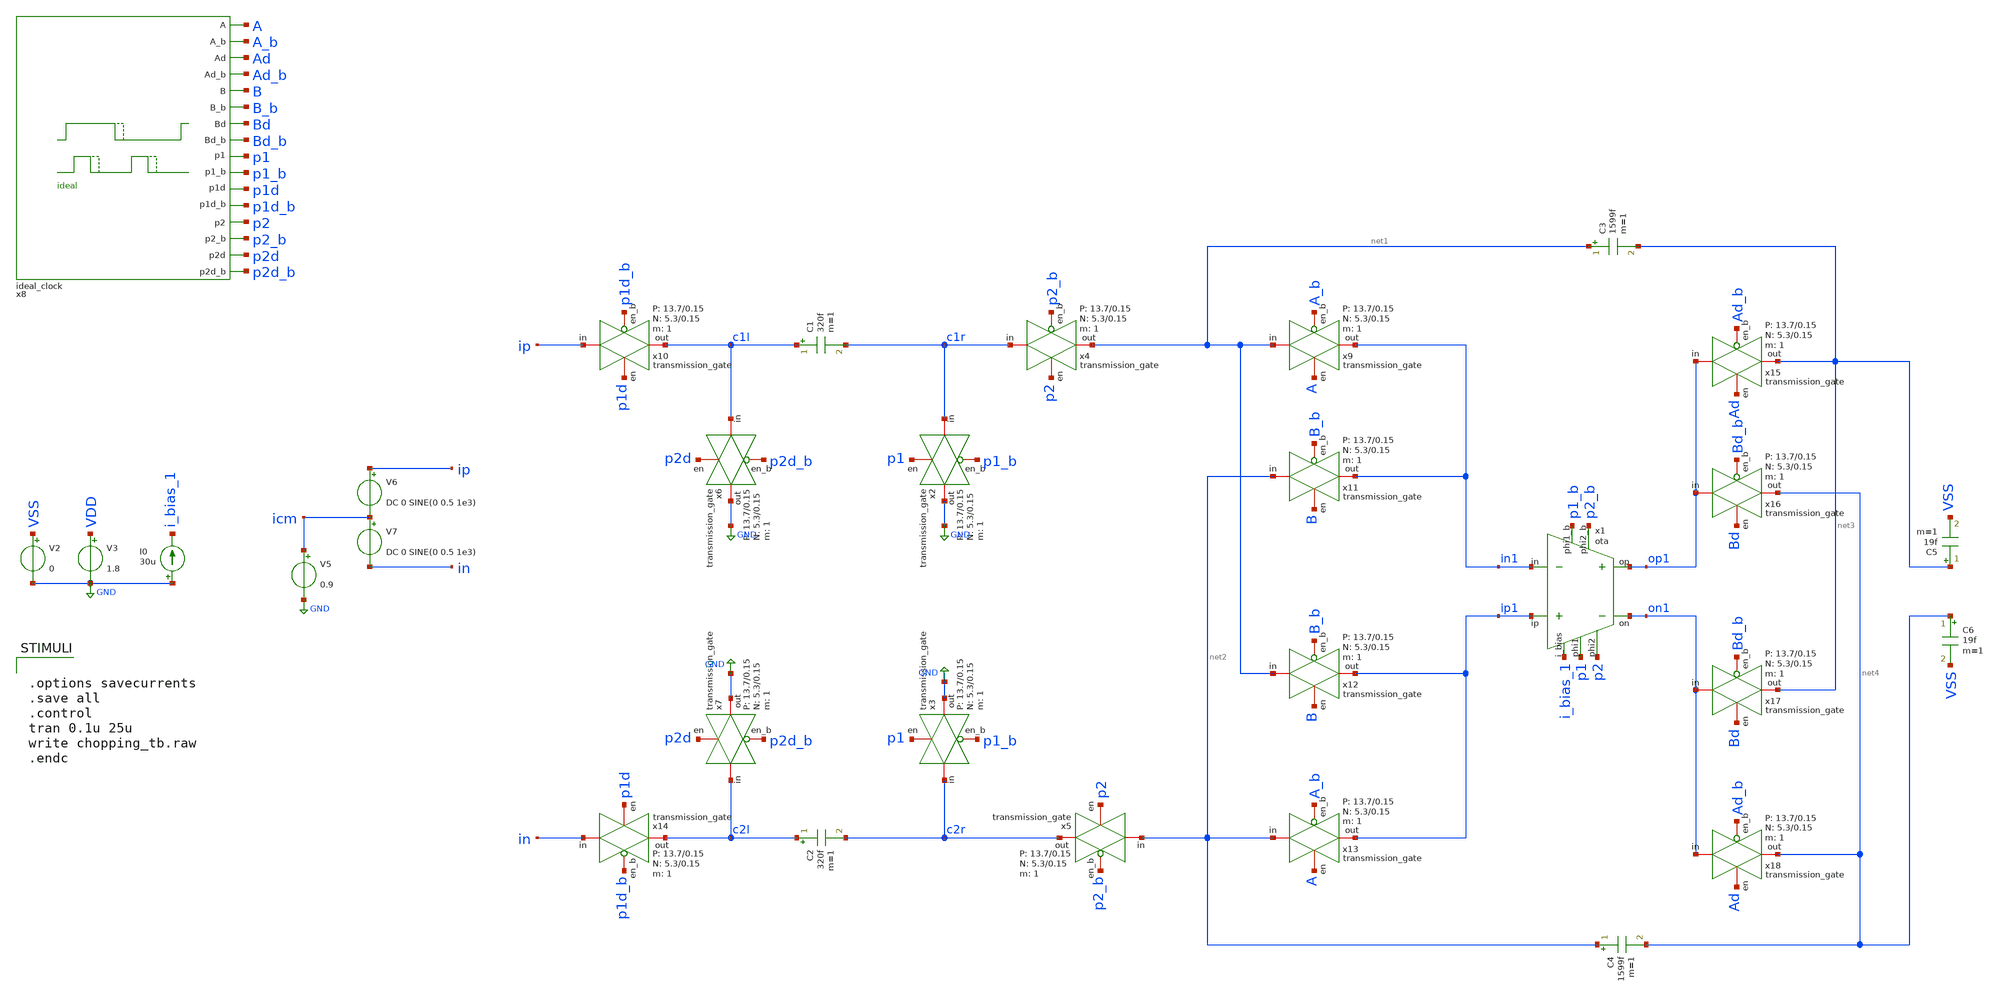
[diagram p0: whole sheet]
** sch_path: verification/analog_modulator/chopping_tb.sch
**.subckt chopping_tb
x4 c1r net1 p2 p2_b VDD VSS 1 5.3 0.15 13.7 0.15 transmission_gate
x5 net2 c2r p2 p2_b VDD VSS 1 5.3 0.15 13.7 0.15 transmission_gate
x2 c1r GND p1 p1_b VDD VSS 1 5.3 0.15 13.7 0.15 transmission_gate
x3 c2r GND p1 p1_b VDD VSS 1 5.3 0.15 13.7 0.15 transmission_gate
C1 c1l c1r 320f m=1
C2 c2l c2r 320f m=1
x10 ip c1l p1d p1d_b VDD VSS 1 5.3 0.15 13.7 0.15 transmission_gate
x14 in c2l p1d p1d_b VDD VSS 1 5.3 0.15 13.7 0.15 transmission_gate
C3 net1 net3 1599f m=1
C4 net2 net4 1599f m=1
V2 VSS GND 0
V3 VDD GND 1.8
x6 c1l GND p2d p2d_b VDD VSS 1 5.3 0.15 13.7 0.15 transmission_gate
x7 c2l GND p2d p2d_b VDD VSS 1 5.3 0.15 13.7 0.15 transmission_gate
x8 A A_b Ad Ad_b Bd_b Bd B_b B p2 p2_b p2d p2d_b p1d_b p1d p1_b p1 0 VDD VSS ideal_clock
x1 i_bias_1 ip1 in1 p1 p1_b p2 p2_b op1 on1 50 350 VDD VSS ota
I0 GND i_bias_1 30u
C5 net3 VSS 19f m=1
C6 net4 VSS 19f m=1
V5 icm GND 0.9
V6 ip icm DC 0 SINE(0 0.5 1e3)
V7 icm in DC 0 SINE(0 0.5 1e3)
x9 net1 in1 A A_b VDD VSS 1 5.3 0.15 13.7 0.15 transmission_gate
x11 net2 in1 B B_b VDD VSS 1 5.3 0.15 13.7 0.15 transmission_gate
x12 net1 ip1 B B_b VDD VSS 1 5.3 0.15 13.7 0.15 transmission_gate
x13 net2 ip1 A A_b VDD VSS 1 5.3 0.15 13.7 0.15 transmission_gate
x15 op1 net3 Ad Ad_b VDD VSS 1 5.3 0.15 13.7 0.15 transmission_gate
x16 op1 net4 Bd Bd_b VDD VSS 1 5.3 0.15 13.7 0.15 transmission_gate
x17 on1 net3 Bd Bd_b VDD VSS 1 5.3 0.15 13.7 0.15 transmission_gate
x18 on1 net4 Ad Ad_b VDD VSS 1 5.3 0.15 13.7 0.15 transmission_gate
**** begin user architecture code

** opencircuitdesign pdks install
.lib /farmshare/home/classes/ee/372/PDKs/open_pdks_1.0.310/sky130/sky130A/libs.tech/ngspice/sky130.lib.spice tt
.inc /farmshare/home/classes/ee/372/PDKs/open_pdks_1.0.310/sky130/sky130A/libs.ref/sky130_fd_sc_hd/spice/sky130_fd_sc_hd.spice



.options savecurrents
.save all
.control
tran 0.1u 25u
write chopping_tb.raw
.endc


**** end user architecture code
**.ends
.GLOBAL GND
.end
